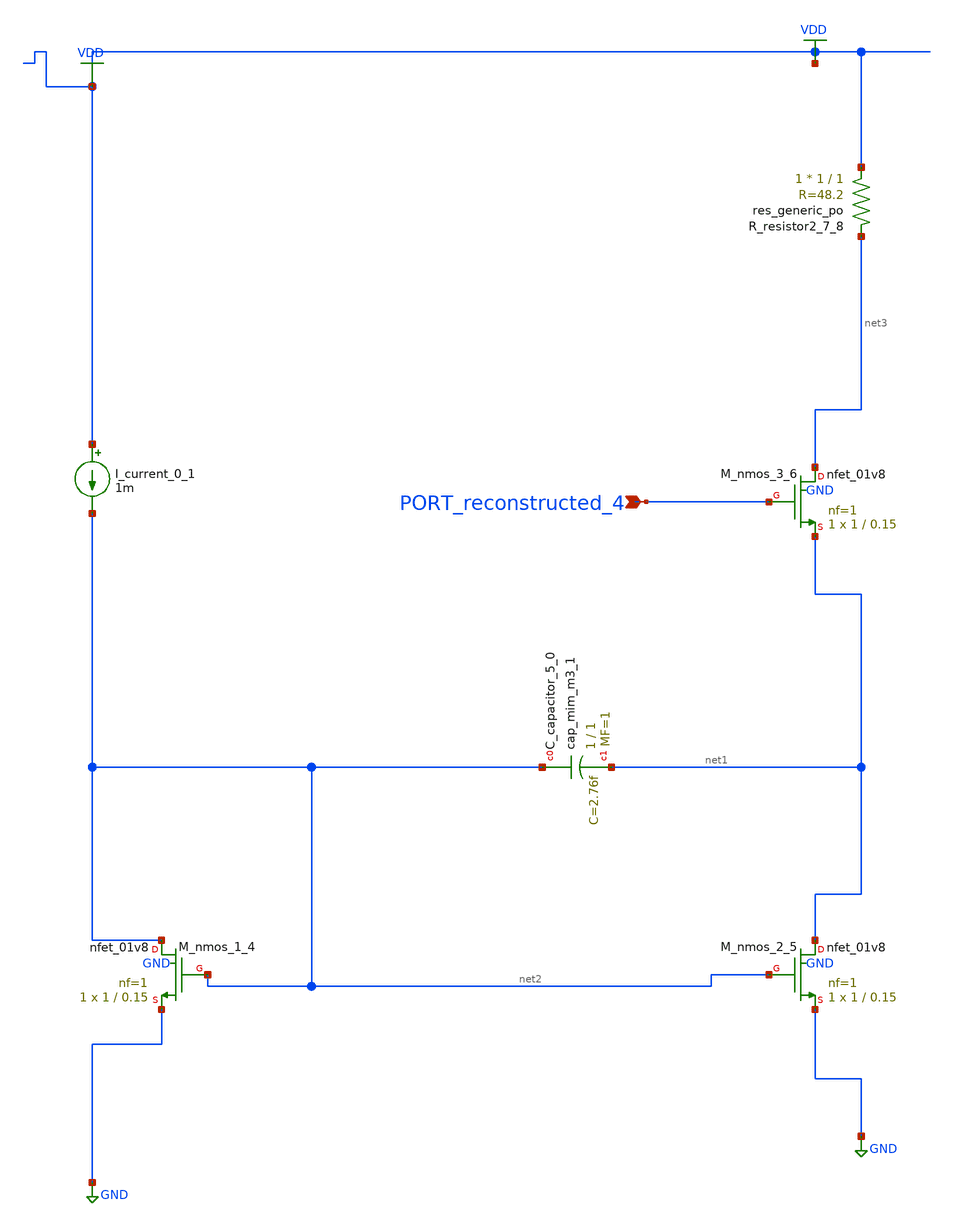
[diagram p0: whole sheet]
** sch_path: schematics/AMSNet/343.sch
**.subckt 343 PORT_reconstructed_4
*.ipin PORT_reconstructed_4
XC_capacitor_5_0 net2 net1 sky130_fd_pr__cap_mim_m3_1 W=1 L=1 MF=1 m=1
I_current_0_1 VDD net2 1m
XM_nmos_1_4 net2 net2 GND GND sky130_fd_pr__nfet_01v8 L=0.15 W=1 nf=1 ad='int((1 + 1)/2) * 1 / 1 * 0.29'
+ as='int((1 + 2)/2) * 1 / 1 * 0.29' pd='2*int((1 + 1)/2) * (1 / 1 + 0.29)' ps='2*int((1 + 2)/2) * (1 / 1 + 0.29)'
+ nrd='0.29 / 1 ' nrs='0.29 / 1 ' sa=0 sb=0 sd=0 mult=1 m=1
XM_nmos_2_5 net1 net2 GND GND sky130_fd_pr__nfet_01v8 L=0.15 W=1 nf=1 ad='int((1 + 1)/2) * 1 / 1 * 0.29'
+ as='int((1 + 2)/2) * 1 / 1 * 0.29' pd='2*int((1 + 1)/2) * (1 / 1 + 0.29)' ps='2*int((1 + 2)/2) * (1 / 1 + 0.29)'
+ nrd='0.29 / 1 ' nrs='0.29 / 1 ' sa=0 sb=0 sd=0 mult=1 m=1
XM_nmos_3_6 net3 PORT_reconstructed_4 net1 GND sky130_fd_pr__nfet_01v8 L=0.15 W=1 nf=1 ad='int((1 + 1)/2) * 1 / 1 * 0.29'
+ as='int((1 + 2)/2) * 1 / 1 * 0.29' pd='2*int((1 + 1)/2) * (1 / 1 + 0.29)' ps='2*int((1 + 2)/2) * (1 / 1 + 0.29)'
+ nrd='0.29 / 1 ' nrs='0.29 / 1 ' sa=0 sb=0 sd=0 mult=1 m=1
XR_resistor2_7_8 VDD net3 sky130_fd_pr__res_generic_po W=1 L=1 m=1
**.ends
.GLOBAL GND
.GLOBAL VDD
.end
